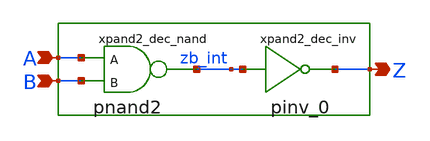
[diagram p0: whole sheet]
** sch_path: sram_2_64_scn4m/and2_dec_0.sch
**.subckt and2_dec_0 A B Z
*.ipin A
*.ipin B
*.opin Z
xpand2_dec_nand A B zb_int vdd gnd pnand2
xpand2_dec_inv zb_int Z vdd gnd pinv_0
**.ends

* expanding   symbol:  pnand2.sym # of pins=3
** sym_path: sram_2_64_scn4m/pnand2.sym
** sch_path: sram_2_64_scn4m/pnand2.sch
.subckt pnand2 A B Z vdd gnd
*.ipin A
*.ipin B
*.opin Z
Mpnand2_nmos1 Z B net1 gnd n w=1.6u l=0.4u m=1
Mpnand2_pmos1 Z A vdd vdd p w=1.6u l=0.4u m=1
Mpnand2_pmos2 Z B vdd vdd p w=1.6u l=0.4u m=1
Mpnand2_nmos2 net1 A gnd gnd n w=1.6u l=0.4u m=1
.ends


* expanding   symbol:  pinv_0.sym # of pins=2
** sym_path: sram_2_16_scn4m/pinv_0.sym
** sch_path: sram_2_16_scn4m/pinv_0.sch
.subckt pinv_0 A Z vdd gnd
*.ipin A
*.opin Z
Mpinv_nmos Z A gnd gnd n w=1.6u l=0.4u m=1
Mp_inv_pmos Z A vdd vdd p w=3.2u l=0.4u m=1
.ends

.end
